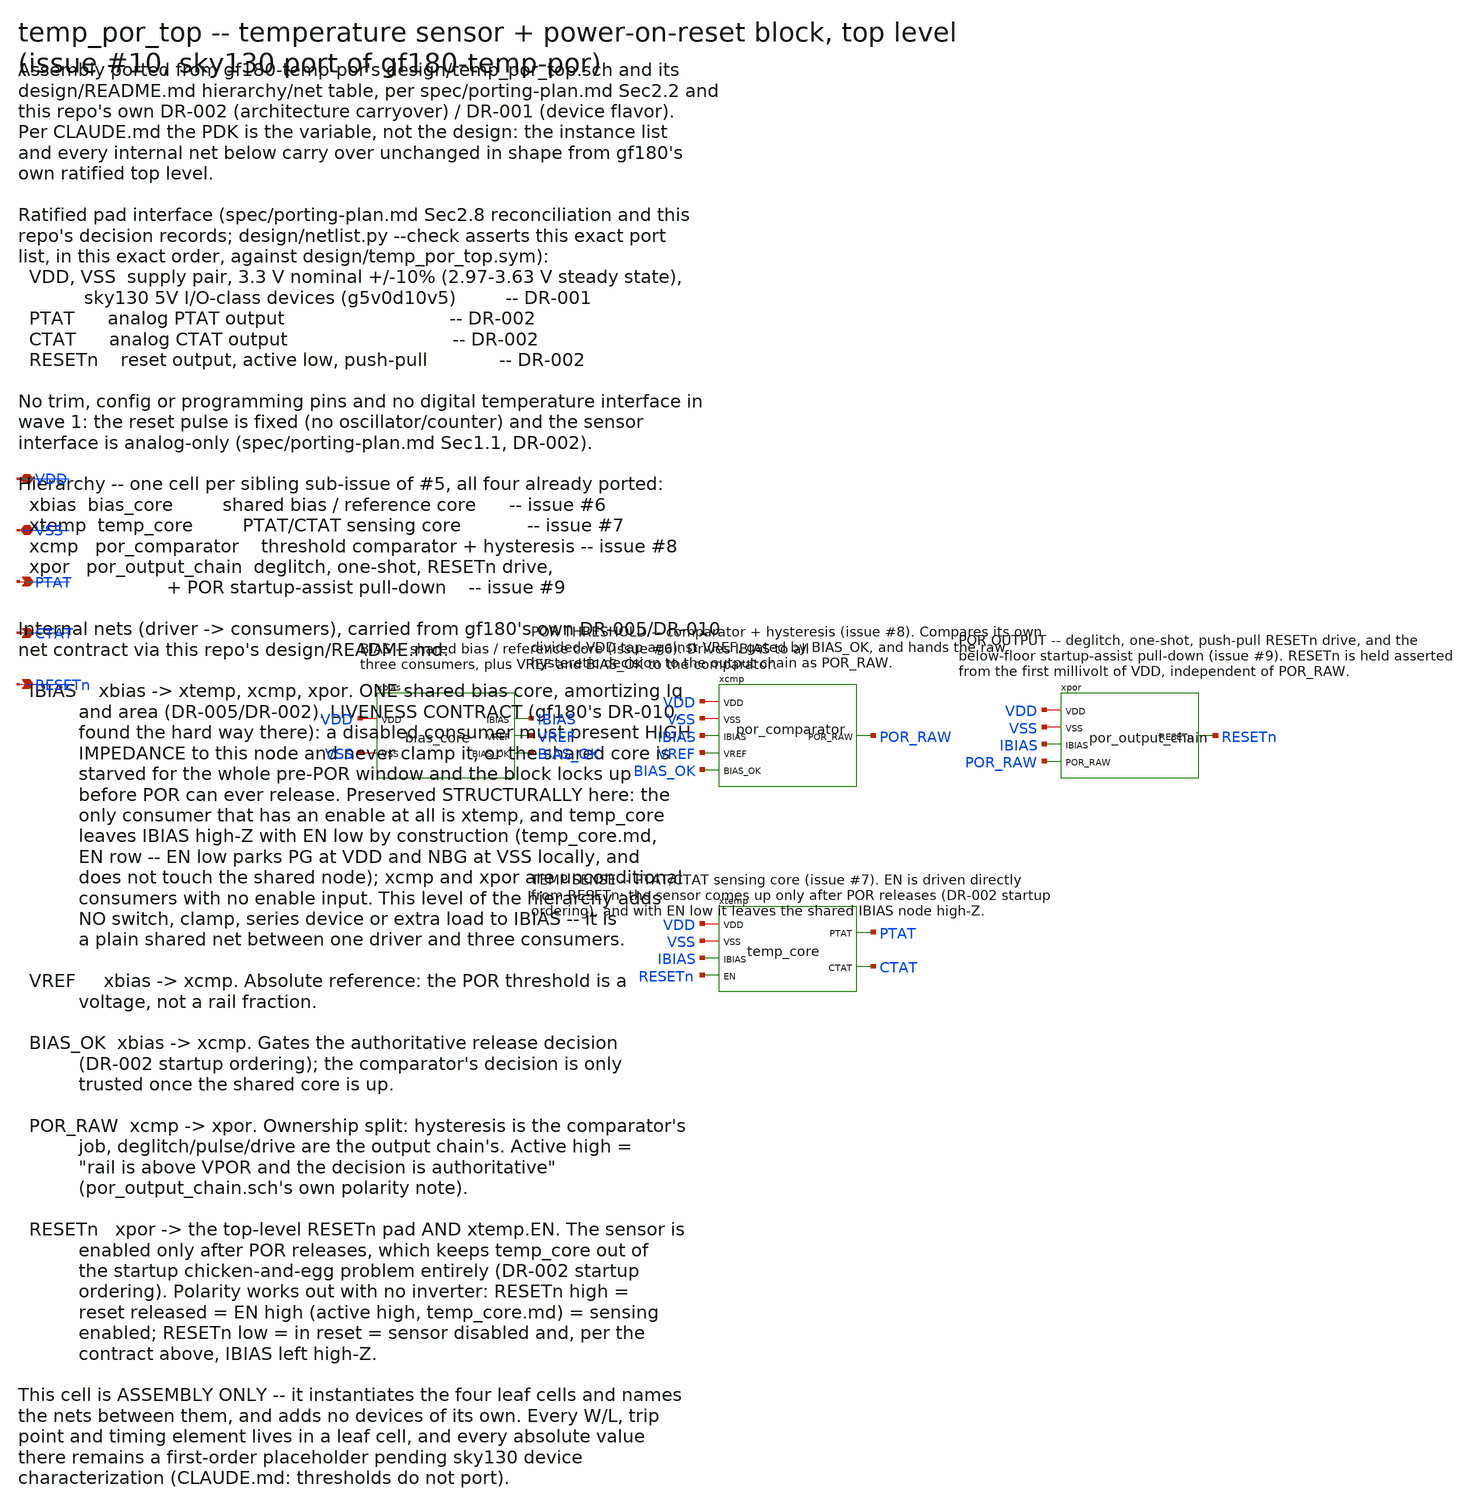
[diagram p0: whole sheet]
** sch_path: design/temp_por_top.sch
**.subckt temp_por_top VDD VSS PTAT CTAT RESETn
*.iopin VDD
*.iopin VSS
*.opin PTAT
*.opin CTAT
*.opin RESETn
xbias VDD VSS IBIAS VREF BIAS_OK bias_core
xcmp VDD VSS IBIAS VREF BIAS_OK POR_RAW por_comparator
xpor VDD VSS IBIAS POR_RAW RESETn por_output_chain
xtemp VDD VSS IBIAS RESETn PTAT CTAT temp_core
**.ends

* expanding   symbol:  bias_core.sym # of pins=5
** sym_path: bias_core.sym
** sch_path: bias_core.sch
.subckt bias_core VDD VSS IBIAS VREF BIAS_OK
*.iopin VDD
*.iopin VSS
*.opin IBIAS
*.opin VREF
*.opin BIAS_OK
XMP1 NA PG VDD VDD sky130_fd_pr__pfet_g5v0d10v5 L=4 W=8 nf=1 ad='int((1 + 1)/2) * 8 / 1 * 0.29' as='int((1 + 2)/2) * 8 / 1 * 0.29'
+ pd='2*int((1 + 1)/2) * (8 / 1 + 0.29)' ps='2*int((1 + 2)/2) * (8 / 1 + 0.29)' nrd='0.29 / 8 ' nrs='0.29 / 8 '
+ sa=0 sb=0 sd=0 mult=1 m=1
XMP2 NBTOP PG VDD VDD sky130_fd_pr__pfet_g5v0d10v5 L=4 W=8 nf=1 ad='int((1 + 1)/2) * 8 / 1 * 0.29' as='int((1 + 2)/2) * 8 / 1 * 0.29'
+ pd='2*int((1 + 1)/2) * (8 / 1 + 0.29)' ps='2*int((1 + 2)/2) * (8 / 1 + 0.29)' nrd='0.29 / 8 ' nrs='0.29 / 8 '
+ sa=0 sb=0 sd=0 mult=1 m=1
XMP3 VREF PG VDD VDD sky130_fd_pr__pfet_g5v0d10v5 L=4 W=8 nf=1 ad='int((1 + 1)/2) * 8 / 1 * 0.29' as='int((1 + 2)/2) * 8 / 1 * 0.29'
+ pd='2*int((1 + 1)/2) * (8 / 1 + 0.29)' ps='2*int((1 + 2)/2) * (8 / 1 + 0.29)' nrd='0.29 / 8 ' nrs='0.29 / 8 '
+ sa=0 sb=0 sd=0 mult=1 m=1
XMPBN NBG PG VDD VDD sky130_fd_pr__pfet_g5v0d10v5 L=4 W=2 nf=1 ad='int((1 + 1)/2) * 2 / 1 * 0.29' as='int((1 + 2)/2) * 2 / 1 * 0.29'
+ pd='2*int((1 + 1)/2) * (2 / 1 + 0.29)' ps='2*int((1 + 2)/2) * (2 / 1 + 0.29)' nrd='0.29 / 2 ' nrs='0.29 / 2 '
+ sa=0 sb=0 sd=0 mult=1 m=1
XQ1 VSS VSS NA sky130_fd_pr__pnp_05v5_W3p40L3p40 m=1
XRT NBTOP NB VSS sky130_fd_pr__res_xhigh_po W=2 L=17.5 mult=1 m=1
XR1 NB EC VSS sky130_fd_pr__res_xhigh_po W=2 L=350.0 mult=1 m=1
XQ8A VSS VSS EC sky130_fd_pr__pnp_05v5_W3p40L3p40 m=1
XQ8B VSS VSS EC sky130_fd_pr__pnp_05v5_W3p40L3p40 m=1
XQ8C VSS VSS EC sky130_fd_pr__pnp_05v5_W3p40L3p40 m=1
XQ8D VSS VSS EC sky130_fd_pr__pnp_05v5_W3p40L3p40 m=1
XQ8E VSS VSS EC sky130_fd_pr__pnp_05v5_W3p40L3p40 m=1
XQ8F VSS VSS EC sky130_fd_pr__pnp_05v5_W3p40L3p40 m=1
XQ8G VSS VSS EC sky130_fd_pr__pnp_05v5_W3p40L3p40 m=1
XQ8H VSS VSS EC sky130_fd_pr__pnp_05v5_W3p40L3p40 m=1
XR2 VREF ER VSS sky130_fd_pr__res_xhigh_po W=2 L=4104.0 mult=1 m=1
XQR VSS VSS ER sky130_fd_pr__pnp_05v5_W3p40L3p40 m=1
XMBN NBG NBG VSS VSS sky130_fd_pr__nfet_g5v0d10v5 L=4 W=2 nf=1 ad='int((1 + 1)/2) * 2 / 1 * 0.29' as='int((1 + 2)/2) * 2 / 1 * 0.29'
+ pd='2*int((1 + 1)/2) * (2 / 1 + 0.29)' ps='2*int((1 + 2)/2) * (2 / 1 + 0.29)' nrd='0.29 / 2 ' nrs='0.29 / 2 '
+ sa=0 sb=0 sd=0 mult=1 m=1
XMBN2 PB NBG VSS VSS sky130_fd_pr__nfet_g5v0d10v5 L=4 W=2 nf=1 ad='int((1 + 1)/2) * 2 / 1 * 0.29' as='int((1 + 2)/2) * 2 / 1 * 0.29'
+ pd='2*int((1 + 1)/2) * (2 / 1 + 0.29)' ps='2*int((1 + 2)/2) * (2 / 1 + 0.29)' nrd='0.29 / 2 ' nrs='0.29 / 2 '
+ sa=0 sb=0 sd=0 mult=1 m=1
XMBP PB PB VDD VDD sky130_fd_pr__pfet_g5v0d10v5 L=4 W=2 nf=1 ad='int((1 + 1)/2) * 2 / 1 * 0.29' as='int((1 + 2)/2) * 2 / 1 * 0.29'
+ pd='2*int((1 + 1)/2) * (2 / 1 + 0.29)' ps='2*int((1 + 2)/2) * (2 / 1 + 0.29)' nrd='0.29 / 2 ' nrs='0.29 / 2 '
+ sa=0 sb=0 sd=0 mult=1 m=1
XMPIB IBIAS PB VDD VDD sky130_fd_pr__pfet_g5v0d10v5 L=4 W=40 nf=1 ad='int((1 + 1)/2) * 40 / 1 * 0.29'
+ as='int((1 + 2)/2) * 40 / 1 * 0.29' pd='2*int((1 + 1)/2) * (40 / 1 + 0.29)' ps='2*int((1 + 2)/2) * (40 / 1 + 0.29)'
+ nrd='0.29 / 40 ' nrs='0.29 / 40 ' sa=0 sb=0 sd=0 mult=1 m=1
XMPT NT PB VDD VDD sky130_fd_pr__pfet_g5v0d10v5 L=4 W=2 nf=1 ad='int((1 + 1)/2) * 2 / 1 * 0.29' as='int((1 + 2)/2) * 2 / 1 * 0.29'
+ pd='2*int((1 + 1)/2) * (2 / 1 + 0.29)' ps='2*int((1 + 2)/2) * (2 / 1 + 0.29)' nrd='0.29 / 2 ' nrs='0.29 / 2 '
+ sa=0 sb=0 sd=0 mult=1 m=1
XMI1 N1 NA NT VDD sky130_fd_pr__pfet_g5v0d10v5 L=4 W=16 nf=1 ad='int((1 + 1)/2) * 16 / 1 * 0.29' as='int((1 + 2)/2) * 16 / 1 * 0.29'
+ pd='2*int((1 + 1)/2) * (16 / 1 + 0.29)' ps='2*int((1 + 2)/2) * (16 / 1 + 0.29)' nrd='0.29 / 16 ' nrs='0.29 / 16 '
+ sa=0 sb=0 sd=0 mult=1 m=1
XMI2 N2 NB NT VDD sky130_fd_pr__pfet_g5v0d10v5 L=4 W=16 nf=1 ad='int((1 + 1)/2) * 16 / 1 * 0.29' as='int((1 + 2)/2) * 16 / 1 * 0.29'
+ pd='2*int((1 + 1)/2) * (16 / 1 + 0.29)' ps='2*int((1 + 2)/2) * (16 / 1 + 0.29)' nrd='0.29 / 16 ' nrs='0.29 / 16 '
+ sa=0 sb=0 sd=0 mult=1 m=1
XML1 N1 N1 VSS VSS sky130_fd_pr__nfet_g5v0d10v5 L=8 W=4 nf=1 ad='int((1 + 1)/2) * 4 / 1 * 0.29' as='int((1 + 2)/2) * 4 / 1 * 0.29'
+ pd='2*int((1 + 1)/2) * (4 / 1 + 0.29)' ps='2*int((1 + 2)/2) * (4 / 1 + 0.29)' nrd='0.29 / 4 ' nrs='0.29 / 4 '
+ sa=0 sb=0 sd=0 mult=1 m=1
XML2 N2 N1 VSS VSS sky130_fd_pr__nfet_g5v0d10v5 L=8 W=4 nf=1 ad='int((1 + 1)/2) * 4 / 1 * 0.29' as='int((1 + 2)/2) * 4 / 1 * 0.29'
+ pd='2*int((1 + 1)/2) * (4 / 1 + 0.29)' ps='2*int((1 + 2)/2) * (4 / 1 + 0.29)' nrd='0.29 / 4 ' nrs='0.29 / 4 '
+ sa=0 sb=0 sd=0 mult=1 m=1
XMS2N PG N2 VSS VSS sky130_fd_pr__nfet_g5v0d10v5 L=8 W=8 nf=1 ad='int((1 + 1)/2) * 8 / 1 * 0.29' as='int((1 + 2)/2) * 8 / 1 * 0.29'
+ pd='2*int((1 + 1)/2) * (8 / 1 + 0.29)' ps='2*int((1 + 2)/2) * (8 / 1 + 0.29)' nrd='0.29 / 8 ' nrs='0.29 / 8 '
+ sa=0 sb=0 sd=0 mult=1 m=1
XMS2P PG PB VDD VDD sky130_fd_pr__pfet_g5v0d10v5 L=4 W=2 nf=1 ad='int((1 + 1)/2) * 2 / 1 * 0.29' as='int((1 + 2)/2) * 2 / 1 * 0.29'
+ pd='2*int((1 + 1)/2) * (2 / 1 + 0.29)' ps='2*int((1 + 2)/2) * (2 / 1 + 0.29)' nrd='0.29 / 2 ' nrs='0.29 / 2 '
+ sa=0 sb=0 sd=0 mult=1 m=1
XCC PG NZ sky130_fd_pr__cap_mim_m3_1 W=20 L=20 MF=1 m=1
XRZ NZ N2 VSS sky130_fd_pr__res_xhigh_po W=2 L=1016.0 mult=1 m=1
XKS0 VDD VDD KS1 VSS sky130_fd_pr__nfet_g5v0d10v5 L=8 W=1 nf=1 ad='int((1 + 1)/2) * 1 / 1 * 0.29' as='int((1 + 2)/2) * 1 / 1 * 0.29'
+ pd='2*int((1 + 1)/2) * (1 / 1 + 0.29)' ps='2*int((1 + 2)/2) * (1 / 1 + 0.29)' nrd='0.29 / 1 ' nrs='0.29 / 1 '
+ sa=0 sb=0 sd=0 mult=1 m=1
XKS1 KS1 KS1 KS2 VSS sky130_fd_pr__nfet_g5v0d10v5 L=8 W=1 nf=1 ad='int((1 + 1)/2) * 1 / 1 * 0.29' as='int((1 + 2)/2) * 1 / 1 * 0.29'
+ pd='2*int((1 + 1)/2) * (1 / 1 + 0.29)' ps='2*int((1 + 2)/2) * (1 / 1 + 0.29)' nrd='0.29 / 1 ' nrs='0.29 / 1 '
+ sa=0 sb=0 sd=0 mult=1 m=1
XKS2 KS2 KS2 KS3 VSS sky130_fd_pr__nfet_g5v0d10v5 L=8 W=1 nf=1 ad='int((1 + 1)/2) * 1 / 1 * 0.29' as='int((1 + 2)/2) * 1 / 1 * 0.29'
+ pd='2*int((1 + 1)/2) * (1 / 1 + 0.29)' ps='2*int((1 + 2)/2) * (1 / 1 + 0.29)' nrd='0.29 / 1 ' nrs='0.29 / 1 '
+ sa=0 sb=0 sd=0 mult=1 m=1
XKS3 KS3 KS3 KS4 VSS sky130_fd_pr__nfet_g5v0d10v5 L=8 W=1 nf=1 ad='int((1 + 1)/2) * 1 / 1 * 0.29' as='int((1 + 2)/2) * 1 / 1 * 0.29'
+ pd='2*int((1 + 1)/2) * (1 / 1 + 0.29)' ps='2*int((1 + 2)/2) * (1 / 1 + 0.29)' nrd='0.29 / 1 ' nrs='0.29 / 1 '
+ sa=0 sb=0 sd=0 mult=1 m=1
XKS4 KS4 KS4 NKG VSS sky130_fd_pr__nfet_g5v0d10v5 L=8 W=1 nf=1 ad='int((1 + 1)/2) * 1 / 1 * 0.29' as='int((1 + 2)/2) * 1 / 1 * 0.29'
+ pd='2*int((1 + 1)/2) * (1 / 1 + 0.29)' ps='2*int((1 + 2)/2) * (1 / 1 + 0.29)' nrd='0.29 / 1 ' nrs='0.29 / 1 '
+ sa=0 sb=0 sd=0 mult=1 m=1
XKA NKM PB VDD VDD sky130_fd_pr__pfet_g5v0d10v5 L=4 W=1 nf=1 ad='int((1 + 1)/2) * 1 / 1 * 0.29' as='int((1 + 2)/2) * 1 / 1 * 0.29'
+ pd='2*int((1 + 1)/2) * (1 / 1 + 0.29)' ps='2*int((1 + 2)/2) * (1 / 1 + 0.29)' nrd='0.29 / 1 ' nrs='0.29 / 1 '
+ sa=0 sb=0 sd=0 mult=1 m=1
XKAN NKM NKM VSS VSS sky130_fd_pr__nfet_g5v0d10v5 L=4 W=2 nf=1 ad='int((1 + 1)/2) * 2 / 1 * 0.29' as='int((1 + 2)/2) * 2 / 1 * 0.29'
+ pd='2*int((1 + 1)/2) * (2 / 1 + 0.29)' ps='2*int((1 + 2)/2) * (2 / 1 + 0.29)' nrd='0.29 / 2 ' nrs='0.29 / 2 '
+ sa=0 sb=0 sd=0 mult=1 m=1
XKPD NKG NKM VSS VSS sky130_fd_pr__nfet_g5v0d10v5 L=4 W=8 nf=1 ad='int((1 + 1)/2) * 8 / 1 * 0.29' as='int((1 + 2)/2) * 8 / 1 * 0.29'
+ pd='2*int((1 + 1)/2) * (8 / 1 + 0.29)' ps='2*int((1 + 2)/2) * (8 / 1 + 0.29)' nrd='0.29 / 8 ' nrs='0.29 / 8 '
+ sa=0 sb=0 sd=0 mult=1 m=1
XKICK PG NKG VSS VSS sky130_fd_pr__nfet_g5v0d10v5 L=4 W=1 nf=1 ad='int((1 + 1)/2) * 1 / 1 * 0.29' as='int((1 + 2)/2) * 1 / 1 * 0.29'
+ pd='2*int((1 + 1)/2) * (1 / 1 + 0.29)' ps='2*int((1 + 2)/2) * (1 / 1 + 0.29)' nrd='0.29 / 1 ' nrs='0.29 / 1 '
+ sa=0 sb=0 sd=0 mult=1 m=1
XMPOK TOK PB VDD VDD sky130_fd_pr__pfet_g5v0d10v5 L=4 W=1 nf=1 ad='int((1 + 1)/2) * 1 / 1 * 0.29' as='int((1 + 2)/2) * 1 / 1 * 0.29'
+ pd='2*int((1 + 1)/2) * (1 / 1 + 0.29)' ps='2*int((1 + 2)/2) * (1 / 1 + 0.29)' nrd='0.29 / 1 ' nrs='0.29 / 1 '
+ sa=0 sb=0 sd=0 mult=1 m=1
XMOKA NOKO NA TOK VDD sky130_fd_pr__pfet_g5v0d10v5 L=4 W=8 nf=1 ad='int((1 + 1)/2) * 8 / 1 * 0.29' as='int((1 + 2)/2) * 8 / 1 * 0.29'
+ pd='2*int((1 + 1)/2) * (8 / 1 + 0.29)' ps='2*int((1 + 2)/2) * (8 / 1 + 0.29)' nrd='0.29 / 8 ' nrs='0.29 / 8 '
+ sa=0 sb=0 sd=0 mult=1 m=1
XMOKB NOKL NBTOP TOK VDD sky130_fd_pr__pfet_g5v0d10v5 L=4 W=8 nf=1 ad='int((1 + 1)/2) * 8 / 1 * 0.29'
+ as='int((1 + 2)/2) * 8 / 1 * 0.29' pd='2*int((1 + 1)/2) * (8 / 1 + 0.29)' ps='2*int((1 + 2)/2) * (8 / 1 + 0.29)'
+ nrd='0.29 / 8 ' nrs='0.29 / 8 ' sa=0 sb=0 sd=0 mult=1 m=1
XMOL1 NOKL NOKL VSS VSS sky130_fd_pr__nfet_g5v0d10v5 L=4 W=2 nf=1 ad='int((1 + 1)/2) * 2 / 1 * 0.29'
+ as='int((1 + 2)/2) * 2 / 1 * 0.29' pd='2*int((1 + 1)/2) * (2 / 1 + 0.29)' ps='2*int((1 + 2)/2) * (2 / 1 + 0.29)'
+ nrd='0.29 / 2 ' nrs='0.29 / 2 ' sa=0 sb=0 sd=0 mult=1 m=1
XMOL2 NOKO NOKL VSS VSS sky130_fd_pr__nfet_g5v0d10v5 L=4 W=2 nf=1 ad='int((1 + 1)/2) * 2 / 1 * 0.29'
+ as='int((1 + 2)/2) * 2 / 1 * 0.29' pd='2*int((1 + 1)/2) * (2 / 1 + 0.29)' ps='2*int((1 + 2)/2) * (2 / 1 + 0.29)'
+ nrd='0.29 / 2 ' nrs='0.29 / 2 ' sa=0 sb=0 sd=0 mult=1 m=1
XMOKC NOKO NKG VSS VSS sky130_fd_pr__nfet_g5v0d10v5 L=1 W=2 nf=1 ad='int((1 + 1)/2) * 2 / 1 * 0.29' as='int((1 + 2)/2) * 2 / 1 * 0.29'
+ pd='2*int((1 + 1)/2) * (2 / 1 + 0.29)' ps='2*int((1 + 2)/2) * (2 / 1 + 0.29)' nrd='0.29 / 2 ' nrs='0.29 / 2 '
+ sa=0 sb=0 sd=0 mult=1 m=1
XMOK2 NOKX NOKO VSS VSS sky130_fd_pr__nfet_g5v0d10v5 L=4 W=2 nf=1 ad='int((1 + 1)/2) * 2 / 1 * 0.29'
+ as='int((1 + 2)/2) * 2 / 1 * 0.29' pd='2*int((1 + 1)/2) * (2 / 1 + 0.29)' ps='2*int((1 + 2)/2) * (2 / 1 + 0.29)'
+ nrd='0.29 / 2 ' nrs='0.29 / 2 ' sa=0 sb=0 sd=0 mult=1 m=1
XMOK2P NOKX PB VDD VDD sky130_fd_pr__pfet_g5v0d10v5 L=4 W=1 nf=1 ad='int((1 + 1)/2) * 1 / 1 * 0.29' as='int((1 + 2)/2) * 1 / 1 * 0.29'
+ pd='2*int((1 + 1)/2) * (1 / 1 + 0.29)' ps='2*int((1 + 2)/2) * (1 / 1 + 0.29)' nrd='0.29 / 1 ' nrs='0.29 / 1 '
+ sa=0 sb=0 sd=0 mult=1 m=1
XCOK VDD NOKX sky130_fd_pr__cap_mim_m3_1 W=6 L=6 MF=1 m=1
XMO1P BIAS_OK NOKX VDD VDD sky130_fd_pr__pfet_g5v0d10v5 L=4 W=1 nf=1 ad='int((1 + 1)/2) * 1 / 1 * 0.29'
+ as='int((1 + 2)/2) * 1 / 1 * 0.29' pd='2*int((1 + 1)/2) * (1 / 1 + 0.29)' ps='2*int((1 + 2)/2) * (1 / 1 + 0.29)'
+ nrd='0.29 / 1 ' nrs='0.29 / 1 ' sa=0 sb=0 sd=0 mult=1 m=1
XMO1N BIAS_OK NOKX VSS VSS sky130_fd_pr__nfet_g5v0d10v5 L=0.5 W=4 nf=1 ad='int((1 + 1)/2) * 4 / 1 * 0.29'
+ as='int((1 + 2)/2) * 4 / 1 * 0.29' pd='2*int((1 + 1)/2) * (4 / 1 + 0.29)' ps='2*int((1 + 2)/2) * (4 / 1 + 0.29)'
+ nrd='0.29 / 4 ' nrs='0.29 / 4 ' sa=0 sb=0 sd=0 mult=1 m=1
.ends


* expanding   symbol:  por_comparator.sym # of pins=6
** sym_path: por_comparator.sym
** sch_path: por_comparator.sch
.subckt por_comparator VDD VSS IBIAS VREF BIAS_OK POR_RAW
*.iopin VDD
*.iopin VSS
*.ipin IBIAS
*.ipin VREF
*.ipin BIAS_OK
*.opin POR_RAW
XMENP BIAS_OKB BIAS_OK VDD VDD sky130_fd_pr__pfet_g5v0d10v5 L=0.5 W=2 nf=1 ad='int((1 + 1)/2) * 2 / 1 * 0.29'
+ as='int((1 + 2)/2) * 2 / 1 * 0.29' pd='2*int((1 + 1)/2) * (2 / 1 + 0.29)' ps='2*int((1 + 2)/2) * (2 / 1 + 0.29)'
+ nrd='0.29 / 2 ' nrs='0.29 / 2 ' sa=0 sb=0 sd=0 mult=1 m=1
XMENN BIAS_OKB BIAS_OK VSS VSS sky130_fd_pr__nfet_g5v0d10v5 L=0.5 W=1 nf=1 ad='int((1 + 1)/2) * 1 / 1 * 0.29'
+ as='int((1 + 2)/2) * 1 / 1 * 0.29' pd='2*int((1 + 1)/2) * (1 / 1 + 0.29)' ps='2*int((1 + 2)/2) * (1 / 1 + 0.29)'
+ nrd='0.29 / 1 ' nrs='0.29 / 1 ' sa=0 sb=0 sd=0 mult=1 m=1
XMBD IBIAS NBG VSS VSS sky130_fd_pr__nfet_g5v0d10v5 L=2 W=2 nf=1 ad='int((1 + 1)/2) * 2 / 1 * 0.29' as='int((1 + 2)/2) * 2 / 1 * 0.29'
+ pd='2*int((1 + 1)/2) * (2 / 1 + 0.29)' ps='2*int((1 + 2)/2) * (2 / 1 + 0.29)' nrd='0.29 / 2 ' nrs='0.29 / 2 '
+ sa=0 sb=0 sd=0 mult=1 m=1
XMPASS IBIAS BIAS_OK NBG VSS sky130_fd_pr__nfet_g5v0d10v5 L=0.5 W=2 nf=1 ad='int((1 + 1)/2) * 2 / 1 * 0.29'
+ as='int((1 + 2)/2) * 2 / 1 * 0.29' pd='2*int((1 + 1)/2) * (2 / 1 + 0.29)' ps='2*int((1 + 2)/2) * (2 / 1 + 0.29)'
+ nrd='0.29 / 2 ' nrs='0.29 / 2 ' sa=0 sb=0 sd=0 mult=1 m=1
XMDNB NBG BIAS_OKB VSS VSS sky130_fd_pr__nfet_g5v0d10v5 L=0.5 W=2 nf=1 ad='int((1 + 1)/2) * 2 / 1 * 0.29'
+ as='int((1 + 2)/2) * 2 / 1 * 0.29' pd='2*int((1 + 1)/2) * (2 / 1 + 0.29)' ps='2*int((1 + 2)/2) * (2 / 1 + 0.29)'
+ nrd='0.29 / 2 ' nrs='0.29 / 2 ' sa=0 sb=0 sd=0 mult=1 m=1
XMDIB IBIAS BIAS_OKB VSS VSS sky130_fd_pr__nfet_g5v0d10v5 L=1 W=1 nf=1 ad='int((1 + 1)/2) * 1 / 1 * 0.29'
+ as='int((1 + 2)/2) * 1 / 1 * 0.29' pd='2*int((1 + 1)/2) * (1 / 1 + 0.29)' ps='2*int((1 + 2)/2) * (1 / 1 + 0.29)'
+ nrd='0.29 / 1 ' nrs='0.29 / 1 ' sa=0 sb=0 sd=0 mult=1 m=1
XRTOP SNS VDD VSS sky130_fd_pr__res_xhigh_po W=2 L=7897.44 mult=1 m=1
XRBOT SNSB SNS VSS sky130_fd_pr__res_xhigh_po W=2 L=6769.23 mult=1 m=1
XRHYS VSS SNSB VSS sky130_fd_pr__res_xhigh_po W=2 L=775.0 mult=1 m=1
XMHSW SNSB N1 VSS VSS sky130_fd_pr__nfet_g5v0d10v5 L=0.5 W=10 nf=1 ad='int((1 + 1)/2) * 10 / 1 * 0.29'
+ as='int((1 + 2)/2) * 10 / 1 * 0.29' pd='2*int((1 + 1)/2) * (10 / 1 + 0.29)' ps='2*int((1 + 2)/2) * (10 / 1 + 0.29)'
+ nrd='0.29 / 10 ' nrs='0.29 / 10 ' sa=0 sb=0 sd=0 mult=1 m=1
XMTAIL TN NBG VSS VSS sky130_fd_pr__nfet_g5v0d10v5 L=10 W=1 nf=1 ad='int((1 + 1)/2) * 1 / 1 * 0.29' as='int((1 + 2)/2) * 1 / 1 * 0.29'
+ pd='2*int((1 + 1)/2) * (1 / 1 + 0.29)' ps='2*int((1 + 2)/2) * (1 / 1 + 0.29)' nrd='0.29 / 1 ' nrs='0.29 / 1 '
+ sa=0 sb=0 sd=0 mult=1 m=1
XMINA NA SNS TN VSS sky130_fd_pr__nfet_g5v0d10v5 L=1 W=2 nf=1 ad='int((1 + 1)/2) * 2 / 1 * 0.29' as='int((1 + 2)/2) * 2 / 1 * 0.29'
+ pd='2*int((1 + 1)/2) * (2 / 1 + 0.29)' ps='2*int((1 + 2)/2) * (2 / 1 + 0.29)' nrd='0.29 / 2 ' nrs='0.29 / 2 '
+ sa=0 sb=0 sd=0 mult=1 m=1
XMINB CMPO VREF TN VSS sky130_fd_pr__nfet_g5v0d10v5 L=1 W=2 nf=1 ad='int((1 + 1)/2) * 2 / 1 * 0.29' as='int((1 + 2)/2) * 2 / 1 * 0.29'
+ pd='2*int((1 + 1)/2) * (2 / 1 + 0.29)' ps='2*int((1 + 2)/2) * (2 / 1 + 0.29)' nrd='0.29 / 2 ' nrs='0.29 / 2 '
+ sa=0 sb=0 sd=0 mult=1 m=1
XMLA NA NA VDDA VDD sky130_fd_pr__pfet_g5v0d10v5 L=1 W=4 nf=1 ad='int((1 + 1)/2) * 4 / 1 * 0.29' as='int((1 + 2)/2) * 4 / 1 * 0.29'
+ pd='2*int((1 + 1)/2) * (4 / 1 + 0.29)' ps='2*int((1 + 2)/2) * (4 / 1 + 0.29)' nrd='0.29 / 4 ' nrs='0.29 / 4 '
+ sa=0 sb=0 sd=0 mult=1 m=1
XMLB CMPO NA VDDA VDD sky130_fd_pr__pfet_g5v0d10v5 L=1 W=4 nf=1 ad='int((1 + 1)/2) * 4 / 1 * 0.29' as='int((1 + 2)/2) * 4 / 1 * 0.29'
+ pd='2*int((1 + 1)/2) * (4 / 1 + 0.29)' ps='2*int((1 + 2)/2) * (4 / 1 + 0.29)' nrd='0.29 / 4 ' nrs='0.29 / 4 '
+ sa=0 sb=0 sd=0 mult=1 m=1
XMENSRC VDDA BIAS_OKB VDD VDD sky130_fd_pr__pfet_g5v0d10v5 L=0.5 W=4 nf=1 ad='int((1 + 1)/2) * 4 / 1 * 0.29'
+ as='int((1 + 2)/2) * 4 / 1 * 0.29' pd='2*int((1 + 1)/2) * (4 / 1 + 0.29)' ps='2*int((1 + 2)/2) * (4 / 1 + 0.29)'
+ nrd='0.29 / 4 ' nrs='0.29 / 4 ' sa=0 sb=0 sd=0 mult=1 m=1
XMDCMPO CMPO BIAS_OKB VSS VSS sky130_fd_pr__nfet_g5v0d10v5 L=1 W=2 nf=1 ad='int((1 + 1)/2) * 2 / 1 * 0.29'
+ as='int((1 + 2)/2) * 2 / 1 * 0.29' pd='2*int((1 + 1)/2) * (2 / 1 + 0.29)' ps='2*int((1 + 2)/2) * (2 / 1 + 0.29)'
+ nrd='0.29 / 2 ' nrs='0.29 / 2 ' sa=0 sb=0 sd=0 mult=1 m=1
XMI1P N1 CMPO VDD VDD sky130_fd_pr__pfet_g5v0d10v5 L=0.5 W=2 nf=1 ad='int((1 + 1)/2) * 2 / 1 * 0.29'
+ as='int((1 + 2)/2) * 2 / 1 * 0.29' pd='2*int((1 + 1)/2) * (2 / 1 + 0.29)' ps='2*int((1 + 2)/2) * (2 / 1 + 0.29)'
+ nrd='0.29 / 2 ' nrs='0.29 / 2 ' sa=0 sb=0 sd=0 mult=1 m=1
XMI1N N1 CMPO VSS VSS sky130_fd_pr__nfet_g5v0d10v5 L=0.5 W=1 nf=1 ad='int((1 + 1)/2) * 1 / 1 * 0.29'
+ as='int((1 + 2)/2) * 1 / 1 * 0.29' pd='2*int((1 + 1)/2) * (1 / 1 + 0.29)' ps='2*int((1 + 2)/2) * (1 / 1 + 0.29)'
+ nrd='0.29 / 1 ' nrs='0.29 / 1 ' sa=0 sb=0 sd=0 mult=1 m=1
XMI2P POR_RAW N1 VDD VDD sky130_fd_pr__pfet_g5v0d10v5 L=0.5 W=2 nf=1 ad='int((1 + 1)/2) * 2 / 1 * 0.29'
+ as='int((1 + 2)/2) * 2 / 1 * 0.29' pd='2*int((1 + 1)/2) * (2 / 1 + 0.29)' ps='2*int((1 + 2)/2) * (2 / 1 + 0.29)'
+ nrd='0.29 / 2 ' nrs='0.29 / 2 ' sa=0 sb=0 sd=0 mult=1 m=1
XMI2N POR_RAW N1 VSS VSS sky130_fd_pr__nfet_g5v0d10v5 L=0.5 W=1 nf=1 ad='int((1 + 1)/2) * 1 / 1 * 0.29'
+ as='int((1 + 2)/2) * 1 / 1 * 0.29' pd='2*int((1 + 1)/2) * (1 / 1 + 0.29)' ps='2*int((1 + 2)/2) * (1 / 1 + 0.29)'
+ nrd='0.29 / 1 ' nrs='0.29 / 1 ' sa=0 sb=0 sd=0 mult=1 m=1
.ends


* expanding   symbol:  por_output_chain.sym # of pins=5
** sym_path: design/por_output_chain.sym
** sch_path: design/por_output_chain.sch
.subckt por_output_chain VDD VSS IBIAS POR_RAW RESETn
*.iopin VDD
*.iopin VSS
*.ipin IBIAS
*.ipin POR_RAW
*.opin RESETn
XMBD IBIAS IBIAS VSS VSS sky130_fd_pr__nfet_g5v0d10v5 L=4 W=4 nf=1 ad='int((1 + 1)/2) * 4 / 1 * 0.29'
+ as='int((1 + 2)/2) * 4 / 1 * 0.29' pd='2*int((1 + 1)/2) * (4 / 1 + 0.29)' ps='2*int((1 + 2)/2) * (4 / 1 + 0.29)'
+ nrd='0.29 / 4 ' nrs='0.29 / 4 ' sa=0 sb=0 sd=0 mult=1 m=1
XMN1 PDN IBIAS VSS VSS sky130_fd_pr__nfet_g5v0d10v5 L=20 W=0.42 nf=1 ad='int((1 + 1)/2) * 0.42 / 1 * 0.29'
+ as='int((1 + 2)/2) * 0.42 / 1 * 0.29' pd='2*int((1 + 1)/2) * (0.42 / 1 + 0.29)' ps='2*int((1 + 2)/2) * (0.42 / 1 + 0.29)'
+ nrd='0.29 / 0.42 ' nrs='0.29 / 0.42 ' sa=0 sb=0 sd=0 mult=1 m=1
XMPD PDN PDN VDD VDD sky130_fd_pr__pfet_g5v0d10v5 L=10 W=2 nf=1 ad='int((1 + 1)/2) * 2 / 1 * 0.29' as='int((1 + 2)/2) * 2 / 1 * 0.29'
+ pd='2*int((1 + 1)/2) * (2 / 1 + 0.29)' ps='2*int((1 + 2)/2) * (2 / 1 + 0.29)' nrd='0.29 / 2 ' nrs='0.29 / 2 '
+ sa=0 sb=0 sd=0 mult=1 m=1
XMP2 NDL PDN VDD VDD sky130_fd_pr__pfet_g5v0d10v5 L=10 W=2 nf=1 ad='int((1 + 1)/2) * 2 / 1 * 0.29' as='int((1 + 2)/2) * 2 / 1 * 0.29'
+ pd='2*int((1 + 1)/2) * (2 / 1 + 0.29)' ps='2*int((1 + 2)/2) * (2 / 1 + 0.29)' nrd='0.29 / 2 ' nrs='0.29 / 2 '
+ sa=0 sb=0 sd=0 mult=1 m=1
XMND NDL NDL VSS VSS sky130_fd_pr__nfet_g5v0d10v5 L=10 W=2 nf=1 ad='int((1 + 1)/2) * 2 / 1 * 0.29' as='int((1 + 2)/2) * 2 / 1 * 0.29'
+ pd='2*int((1 + 1)/2) * (2 / 1 + 0.29)' ps='2*int((1 + 2)/2) * (2 / 1 + 0.29)' nrd='0.29 / 2 ' nrs='0.29 / 2 '
+ sa=0 sb=0 sd=0 mult=1 m=1
XMDGPT NDGP PDN VDD VDD sky130_fd_pr__pfet_g5v0d10v5 L=10 W=10 nf=1 ad='int((1 + 1)/2) * 10 / 1 * 0.29'
+ as='int((1 + 2)/2) * 10 / 1 * 0.29' pd='2*int((1 + 1)/2) * (10 / 1 + 0.29)' ps='2*int((1 + 2)/2) * (10 / 1 + 0.29)'
+ nrd='0.29 / 10 ' nrs='0.29 / 10 ' sa=0 sb=0 sd=0 mult=1 m=1
XMDGPI NDG POR_RAW NDGP VDD sky130_fd_pr__pfet_g5v0d10v5 L=0.5 W=1 nf=1 ad='int((1 + 1)/2) * 1 / 1 * 0.29'
+ as='int((1 + 2)/2) * 1 / 1 * 0.29' pd='2*int((1 + 1)/2) * (1 / 1 + 0.29)' ps='2*int((1 + 2)/2) * (1 / 1 + 0.29)'
+ nrd='0.29 / 1 ' nrs='0.29 / 1 ' sa=0 sb=0 sd=0 mult=1 m=1
XMDGNI NDG POR_RAW NDGN VSS sky130_fd_pr__nfet_g5v0d10v5 L=0.5 W=1 nf=1 ad='int((1 + 1)/2) * 1 / 1 * 0.29'
+ as='int((1 + 2)/2) * 1 / 1 * 0.29' pd='2*int((1 + 1)/2) * (1 / 1 + 0.29)' ps='2*int((1 + 2)/2) * (1 / 1 + 0.29)'
+ nrd='0.29 / 1 ' nrs='0.29 / 1 ' sa=0 sb=0 sd=0 mult=1 m=1
XMDGNT NDGN NDL VSS VSS sky130_fd_pr__nfet_g5v0d10v5 L=10 W=10 nf=1 ad='int((1 + 1)/2) * 10 / 1 * 0.29'
+ as='int((1 + 2)/2) * 10 / 1 * 0.29' pd='2*int((1 + 1)/2) * (10 / 1 + 0.29)' ps='2*int((1 + 2)/2) * (10 / 1 + 0.29)'
+ nrd='0.29 / 10 ' nrs='0.29 / 10 ' sa=0 sb=0 sd=0 mult=1 m=1
XCDG NDG VSS sky130_fd_pr__cap_mim_m3_1 W=11 L=11 MF=1 m=1
XMG1P PGDG NDG VDD VDD sky130_fd_pr__pfet_g5v0d10v5 L=2 W=0.5 nf=1 ad='int((1 + 1)/2) * 0.5 / 1 * 0.29'
+ as='int((1 + 2)/2) * 0.5 / 1 * 0.29' pd='2*int((1 + 1)/2) * (0.5 / 1 + 0.29)' ps='2*int((1 + 2)/2) * (0.5 / 1 + 0.29)'
+ nrd='0.29 / 0.5 ' nrs='0.29 / 0.5 ' sa=0 sb=0 sd=0 mult=1 m=1
XMG1N PGDG NDG VSS VSS sky130_fd_pr__nfet_g5v0d10v5 L=0.5 W=2 nf=1 ad='int((1 + 1)/2) * 2 / 1 * 0.29'
+ as='int((1 + 2)/2) * 2 / 1 * 0.29' pd='2*int((1 + 1)/2) * (2 / 1 + 0.29)' ps='2*int((1 + 2)/2) * (2 / 1 + 0.29)'
+ nrd='0.29 / 2 ' nrs='0.29 / 2 ' sa=0 sb=0 sd=0 mult=1 m=1
XMG2P PGDGB PGDG VDD VDD sky130_fd_pr__pfet_g5v0d10v5 L=0.5 W=2 nf=1 ad='int((1 + 1)/2) * 2 / 1 * 0.29'
+ as='int((1 + 2)/2) * 2 / 1 * 0.29' pd='2*int((1 + 1)/2) * (2 / 1 + 0.29)' ps='2*int((1 + 2)/2) * (2 / 1 + 0.29)'
+ nrd='0.29 / 2 ' nrs='0.29 / 2 ' sa=0 sb=0 sd=0 mult=1 m=1
XMG2N PGDGB PGDG VSS VSS sky130_fd_pr__nfet_g5v0d10v5 L=2 W=0.5 nf=1 ad='int((1 + 1)/2) * 0.5 / 1 * 0.29'
+ as='int((1 + 2)/2) * 0.5 / 1 * 0.29' pd='2*int((1 + 1)/2) * (0.5 / 1 + 0.29)' ps='2*int((1 + 2)/2) * (0.5 / 1 + 0.29)'
+ nrd='0.29 / 0.5 ' nrs='0.29 / 0.5 ' sa=0 sb=0 sd=0 mult=1 m=1
XMPT NTS PDN VDD VDD sky130_fd_pr__pfet_g5v0d10v5 L=10 W=0.5 nf=1 ad='int((1 + 1)/2) * 0.5 / 1 * 0.29'
+ as='int((1 + 2)/2) * 0.5 / 1 * 0.29' pd='2*int((1 + 1)/2) * (0.5 / 1 + 0.29)' ps='2*int((1 + 2)/2) * (0.5 / 1 + 0.29)'
+ nrd='0.29 / 0.5 ' nrs='0.29 / 0.5 ' sa=0 sb=0 sd=0 mult=1 m=1
XMTSW TIM PGDGB NTS VDD sky130_fd_pr__pfet_g5v0d10v5 L=1 W=2 nf=1 ad='int((1 + 1)/2) * 2 / 1 * 0.29'
+ as='int((1 + 2)/2) * 2 / 1 * 0.29' pd='2*int((1 + 1)/2) * (2 / 1 + 0.29)' ps='2*int((1 + 2)/2) * (2 / 1 + 0.29)'
+ nrd='0.29 / 2 ' nrs='0.29 / 2 ' sa=0 sb=0 sd=0 mult=1 m=1
XMDIS TIM PGDGB VSS VSS sky130_fd_pr__nfet_g5v0d10v5 L=1 W=1 nf=1 ad='int((1 + 1)/2) * 1 / 1 * 0.29'
+ as='int((1 + 2)/2) * 1 / 1 * 0.29' pd='2*int((1 + 1)/2) * (1 / 1 + 0.29)' ps='2*int((1 + 2)/2) * (1 / 1 + 0.29)'
+ nrd='0.29 / 1 ' nrs='0.29 / 1 ' sa=0 sb=0 sd=0 mult=1 m=1
XCTIM TIM VSS sky130_fd_pr__cap_mim_m3_1 W=28 L=28 MF=4 m=4
XMDAPI ND1 TIM VDD VDD sky130_fd_pr__pfet_g5v0d10v5 L=1 W=2 nf=1 ad='int((1 + 1)/2) * 2 / 1 * 0.29' as='int((1 + 2)/2) * 2 / 1 * 0.29'
+ pd='2*int((1 + 1)/2) * (2 / 1 + 0.29)' ps='2*int((1 + 2)/2) * (2 / 1 + 0.29)' nrd='0.29 / 2 ' nrs='0.29 / 2 '
+ sa=0 sb=0 sd=0 mult=1 m=1
XMDANT ND1 NDL VSS VSS sky130_fd_pr__nfet_g5v0d10v5 L=10 W=0.5 nf=1 ad='int((1 + 1)/2) * 0.5 / 1 * 0.29'
+ as='int((1 + 2)/2) * 0.5 / 1 * 0.29' pd='2*int((1 + 1)/2) * (0.5 / 1 + 0.29)' ps='2*int((1 + 2)/2) * (0.5 / 1 + 0.29)'
+ nrd='0.29 / 0.5 ' nrs='0.29 / 0.5 ' sa=0 sb=0 sd=0 mult=1 m=1
XMDBNI TRIP ND1 VSS VSS sky130_fd_pr__nfet_g5v0d10v5 L=1 W=1 nf=1 ad='int((1 + 1)/2) * 1 / 1 * 0.29'
+ as='int((1 + 2)/2) * 1 / 1 * 0.29' pd='2*int((1 + 1)/2) * (1 / 1 + 0.29)' ps='2*int((1 + 2)/2) * (1 / 1 + 0.29)'
+ nrd='0.29 / 1 ' nrs='0.29 / 1 ' sa=0 sb=0 sd=0 mult=1 m=1
XMDBPT TRIP PDN VDD VDD sky130_fd_pr__pfet_g5v0d10v5 L=10 W=0.5 nf=1 ad='int((1 + 1)/2) * 0.5 / 1 * 0.29'
+ as='int((1 + 2)/2) * 0.5 / 1 * 0.29' pd='2*int((1 + 1)/2) * (0.5 / 1 + 0.29)' ps='2*int((1 + 2)/2) * (0.5 / 1 + 0.29)'
+ nrd='0.29 / 0.5 ' nrs='0.29 / 0.5 ' sa=0 sb=0 sd=0 mult=1 m=1
XMRLK ND1 RESETn VSS VSS sky130_fd_pr__nfet_g5v0d10v5 L=1 W=1 nf=1 ad='int((1 + 1)/2) * 1 / 1 * 0.29'
+ as='int((1 + 2)/2) * 1 / 1 * 0.29' pd='2*int((1 + 1)/2) * (1 / 1 + 0.29)' ps='2*int((1 + 2)/2) * (1 / 1 + 0.29)'
+ nrd='0.29 / 1 ' nrs='0.29 / 1 ' sa=0 sb=0 sd=0 mult=1 m=1
XMNAP1 RSTB TRIP VDD VDD sky130_fd_pr__pfet_g5v0d10v5 L=0.5 W=4 nf=1 ad='int((1 + 1)/2) * 4 / 1 * 0.29'
+ as='int((1 + 2)/2) * 4 / 1 * 0.29' pd='2*int((1 + 1)/2) * (4 / 1 + 0.29)' ps='2*int((1 + 2)/2) * (4 / 1 + 0.29)'
+ nrd='0.29 / 4 ' nrs='0.29 / 4 ' sa=0 sb=0 sd=0 mult=1 m=1
XMNAP2 RSTB PGDG VDD VDD sky130_fd_pr__pfet_g5v0d10v5 L=0.5 W=4 nf=1 ad='int((1 + 1)/2) * 4 / 1 * 0.29'
+ as='int((1 + 2)/2) * 4 / 1 * 0.29' pd='2*int((1 + 1)/2) * (4 / 1 + 0.29)' ps='2*int((1 + 2)/2) * (4 / 1 + 0.29)'
+ nrd='0.29 / 4 ' nrs='0.29 / 4 ' sa=0 sb=0 sd=0 mult=1 m=1
XMNAN1 RSTB TRIP NNAND VSS sky130_fd_pr__nfet_g5v0d10v5 L=0.5 W=2 nf=1 ad='int((1 + 1)/2) * 2 / 1 * 0.29'
+ as='int((1 + 2)/2) * 2 / 1 * 0.29' pd='2*int((1 + 1)/2) * (2 / 1 + 0.29)' ps='2*int((1 + 2)/2) * (2 / 1 + 0.29)'
+ nrd='0.29 / 2 ' nrs='0.29 / 2 ' sa=0 sb=0 sd=0 mult=1 m=1
XMNAN2 NNAND PGDG VSS VSS sky130_fd_pr__nfet_g5v0d10v5 L=0.5 W=2 nf=1 ad='int((1 + 1)/2) * 2 / 1 * 0.29'
+ as='int((1 + 2)/2) * 2 / 1 * 0.29' pd='2*int((1 + 1)/2) * (2 / 1 + 0.29)' ps='2*int((1 + 2)/2) * (2 / 1 + 0.29)'
+ nrd='0.29 / 2 ' nrs='0.29 / 2 ' sa=0 sb=0 sd=0 mult=1 m=1
XMAST RSTB RESETn VDD VDD sky130_fd_pr__pfet_g5v0d10v5 L=10 W=0.5 nf=1 ad='int((1 + 1)/2) * 0.5 / 1 * 0.29'
+ as='int((1 + 2)/2) * 0.5 / 1 * 0.29' pd='2*int((1 + 1)/2) * (0.5 / 1 + 0.29)' ps='2*int((1 + 2)/2) * (0.5 / 1 + 0.29)'
+ nrd='0.29 / 0.5 ' nrs='0.29 / 0.5 ' sa=0 sb=0 sd=0 mult=1 m=1
XMOP RESETn RSTB VDD VDD sky130_fd_pr__pfet_g5v0d10v5 L=1 W=1 nf=1 ad='int((1 + 1)/2) * 1 / 1 * 0.29'
+ as='int((1 + 2)/2) * 1 / 1 * 0.29' pd='2*int((1 + 1)/2) * (1 / 1 + 0.29)' ps='2*int((1 + 2)/2) * (1 / 1 + 0.29)'
+ nrd='0.29 / 1 ' nrs='0.29 / 1 ' sa=0 sb=0 sd=0 mult=1 m=1
XMON RESETn RSTB VSS VSS sky130_fd_pr__nfet_g5v0d10v5 L=0.5 W=10 nf=1 ad='int((1 + 1)/2) * 10 / 1 * 0.29'
+ as='int((1 + 2)/2) * 10 / 1 * 0.29' pd='2*int((1 + 1)/2) * (10 / 1 + 0.29)' ps='2*int((1 + 2)/2) * (10 / 1 + 0.29)'
+ nrd='0.29 / 10 ' nrs='0.29 / 10 ' sa=0 sb=0 sd=0 mult=1 m=1
XMASSIST RESETn VDD VSS VSS sky130_fd_pr__nfet_05v0_nvt L=25 W=1 nf=1 ad='int((1 + 1)/2) * 1 / 1 * 0.29'
+ as='int((1 + 2)/2) * 1 / 1 * 0.29' pd='2*int((1 + 1)/2) * (1 / 1 + 0.29)' ps='2*int((1 + 2)/2) * (1 / 1 + 0.29)'
+ nrd='0.29 / 1 ' nrs='0.29 / 1 ' sa=0 sb=0 sd=0 mult=1 m=1
.ends


* expanding   symbol:  temp_core.sym # of pins=6
** sym_path: temp_core.sym
** sch_path: temp_core.sch
.subckt temp_core VDD VSS IBIAS EN PTAT CTAT
*.iopin VDD
*.iopin VSS
*.ipin IBIAS
*.ipin EN
*.opin PTAT
*.opin CTAT
XMBD IBIAS NBG VSS VSS sky130_fd_pr__nfet_g5v0d10v5 L=2 W=4 nf=1 ad='int((1 + 1)/2) * 4 / 1 * 0.29' as='int((1 + 2)/2) * 4 / 1 * 0.29'
+ pd='2*int((1 + 1)/2) * (4 / 1 + 0.29)' ps='2*int((1 + 2)/2) * (4 / 1 + 0.29)' nrd='0.29 / 4 ' nrs='0.29 / 4 '
+ sa=0 sb=0 sd=0 mult=1 m=1
XMPASS IBIAS EN NBG VSS sky130_fd_pr__nfet_g5v0d10v5 L=0.5 W=2 nf=1 ad='int((1 + 1)/2) * 2 / 1 * 0.29'
+ as='int((1 + 2)/2) * 2 / 1 * 0.29' pd='2*int((1 + 1)/2) * (2 / 1 + 0.29)' ps='2*int((1 + 2)/2) * (2 / 1 + 0.29)'
+ nrd='0.29 / 2 ' nrs='0.29 / 2 ' sa=0 sb=0 sd=0 mult=1 m=1
XMDNB NBG ENB VSS VSS sky130_fd_pr__nfet_g5v0d10v5 L=0.5 W=2 nf=1 ad='int((1 + 1)/2) * 2 / 1 * 0.29'
+ as='int((1 + 2)/2) * 2 / 1 * 0.29' pd='2*int((1 + 1)/2) * (2 / 1 + 0.29)' ps='2*int((1 + 2)/2) * (2 / 1 + 0.29)'
+ nrd='0.29 / 2 ' nrs='0.29 / 2 ' sa=0 sb=0 sd=0 mult=1 m=1
XMBN1 PB NBG VSS VSS sky130_fd_pr__nfet_g5v0d10v5 L=2 W=4 nf=1 ad='int((1 + 1)/2) * 4 / 1 * 0.29' as='int((1 + 2)/2) * 4 / 1 * 0.29'
+ pd='2*int((1 + 1)/2) * (4 / 1 + 0.29)' ps='2*int((1 + 2)/2) * (4 / 1 + 0.29)' nrd='0.29 / 4 ' nrs='0.29 / 4 '
+ sa=0 sb=0 sd=0 mult=1 m=1
XMBP PB PB VDD VDD sky130_fd_pr__pfet_g5v0d10v5 L=4 W=10 nf=1 ad='int((1 + 1)/2) * 10 / 1 * 0.29' as='int((1 + 2)/2) * 10 / 1 * 0.29'
+ pd='2*int((1 + 1)/2) * (10 / 1 + 0.29)' ps='2*int((1 + 2)/2) * (10 / 1 + 0.29)' nrd='0.29 / 10 ' nrs='0.29 / 10 '
+ sa=0 sb=0 sd=0 mult=1 m=1
XMBN2 PCAS NBG VSS VSS sky130_fd_pr__nfet_g5v0d10v5 L=2 W=4 nf=1 ad='int((1 + 1)/2) * 4 / 1 * 0.29' as='int((1 + 2)/2) * 4 / 1 * 0.29'
+ pd='2*int((1 + 1)/2) * (4 / 1 + 0.29)' ps='2*int((1 + 2)/2) * (4 / 1 + 0.29)' nrd='0.29 / 4 ' nrs='0.29 / 4 '
+ sa=0 sb=0 sd=0 mult=1 m=1
XMCB PCAS PCAS VDD VDD sky130_fd_pr__pfet_g5v0d10v5 L=8 W=1 nf=1 ad='int((1 + 1)/2) * 1 / 1 * 0.29' as='int((1 + 2)/2) * 1 / 1 * 0.29'
+ pd='2*int((1 + 1)/2) * (1 / 1 + 0.29)' ps='2*int((1 + 2)/2) * (1 / 1 + 0.29)' nrd='0.29 / 1 ' nrs='0.29 / 1 '
+ sa=0 sb=0 sd=0 mult=1 m=1
XMINVP ENB EN VDD VDD sky130_fd_pr__pfet_g5v0d10v5 L=0.5 W=2 nf=1 ad='int((1 + 1)/2) * 2 / 1 * 0.29'
+ as='int((1 + 2)/2) * 2 / 1 * 0.29' pd='2*int((1 + 1)/2) * (2 / 1 + 0.29)' ps='2*int((1 + 2)/2) * (2 / 1 + 0.29)'
+ nrd='0.29 / 2 ' nrs='0.29 / 2 ' sa=0 sb=0 sd=0 mult=1 m=1
XMINVN ENB EN VSS VSS sky130_fd_pr__nfet_g5v0d10v5 L=0.5 W=1 nf=1 ad='int((1 + 1)/2) * 1 / 1 * 0.29'
+ as='int((1 + 2)/2) * 1 / 1 * 0.29' pd='2*int((1 + 1)/2) * (1 / 1 + 0.29)' ps='2*int((1 + 2)/2) * (1 / 1 + 0.29)'
+ nrd='0.29 / 1 ' nrs='0.29 / 1 ' sa=0 sb=0 sd=0 mult=1 m=1
XMT NT PB VDD VDD sky130_fd_pr__pfet_g5v0d10v5 L=4 W=20 nf=1 ad='int((1 + 1)/2) * 20 / 1 * 0.29' as='int((1 + 2)/2) * 20 / 1 * 0.29'
+ pd='2*int((1 + 1)/2) * (20 / 1 + 0.29)' ps='2*int((1 + 2)/2) * (20 / 1 + 0.29)' nrd='0.29 / 20 ' nrs='0.29 / 20 '
+ sa=0 sb=0 sd=0 mult=1 m=1
XMI1 N1 NA NT NT sky130_fd_pr__pfet_g5v0d10v5 L=4 W=32 nf=1 ad='int((1 + 1)/2) * 32 / 1 * 0.29' as='int((1 + 2)/2) * 32 / 1 * 0.29'
+ pd='2*int((1 + 1)/2) * (32 / 1 + 0.29)' ps='2*int((1 + 2)/2) * (32 / 1 + 0.29)' nrd='0.29 / 32 ' nrs='0.29 / 32 '
+ sa=0 sb=0 sd=0 mult=1 m=1
XMI2 N2 NB NT NT sky130_fd_pr__pfet_g5v0d10v5 L=4 W=32 nf=1 ad='int((1 + 1)/2) * 32 / 1 * 0.29' as='int((1 + 2)/2) * 32 / 1 * 0.29'
+ pd='2*int((1 + 1)/2) * (32 / 1 + 0.29)' ps='2*int((1 + 2)/2) * (32 / 1 + 0.29)' nrd='0.29 / 32 ' nrs='0.29 / 32 '
+ sa=0 sb=0 sd=0 mult=1 m=1
XML1 N1 N1 VSS VSS sky130_fd_pr__nfet_g5v0d10v5 L=8 W=8 nf=1 ad='int((1 + 1)/2) * 8 / 1 * 0.29' as='int((1 + 2)/2) * 8 / 1 * 0.29'
+ pd='2*int((1 + 1)/2) * (8 / 1 + 0.29)' ps='2*int((1 + 2)/2) * (8 / 1 + 0.29)' nrd='0.29 / 8 ' nrs='0.29 / 8 '
+ sa=0 sb=0 sd=0 mult=1 m=1
XML2 N2 N1 VSS VSS sky130_fd_pr__nfet_g5v0d10v5 L=8 W=8 nf=1 ad='int((1 + 1)/2) * 8 / 1 * 0.29' as='int((1 + 2)/2) * 8 / 1 * 0.29'
+ pd='2*int((1 + 1)/2) * (8 / 1 + 0.29)' ps='2*int((1 + 2)/2) * (8 / 1 + 0.29)' nrd='0.29 / 8 ' nrs='0.29 / 8 '
+ sa=0 sb=0 sd=0 mult=1 m=1
XMS2N PG N2 VSS VSS sky130_fd_pr__nfet_g5v0d10v5 L=8 W=8 nf=1 ad='int((1 + 1)/2) * 8 / 1 * 0.29' as='int((1 + 2)/2) * 8 / 1 * 0.29'
+ pd='2*int((1 + 1)/2) * (8 / 1 + 0.29)' ps='2*int((1 + 2)/2) * (8 / 1 + 0.29)' nrd='0.29 / 8 ' nrs='0.29 / 8 '
+ sa=0 sb=0 sd=0 mult=1 m=1
XMS2P PG PB VDD VDD sky130_fd_pr__pfet_g5v0d10v5 L=4 W=10 nf=1 ad='int((1 + 1)/2) * 10 / 1 * 0.29' as='int((1 + 2)/2) * 10 / 1 * 0.29'
+ pd='2*int((1 + 1)/2) * (10 / 1 + 0.29)' ps='2*int((1 + 2)/2) * (10 / 1 + 0.29)' nrd='0.29 / 10 ' nrs='0.29 / 10 '
+ sa=0 sb=0 sd=0 mult=1 m=1
XCC PG NZ sky130_fd_pr__cap_mim_m3_1 W=12 L=12 MF=1 m=1
XRZ NZ N2 VSS sky130_fd_pr__res_xhigh_po W=2 L=1000 mult=1 m=1
XMP1 M1D PG VDD VDD sky130_fd_pr__pfet_g5v0d10v5 L=4 W=8 nf=1 ad='int((1 + 1)/2) * 8 / 1 * 0.29' as='int((1 + 2)/2) * 8 / 1 * 0.29'
+ pd='2*int((1 + 1)/2) * (8 / 1 + 0.29)' ps='2*int((1 + 2)/2) * (8 / 1 + 0.29)' nrd='0.29 / 8 ' nrs='0.29 / 8 '
+ sa=0 sb=0 sd=0 mult=1 m=1
XMPC1 NA PCAS M1D VDD sky130_fd_pr__pfet_g5v0d10v5 L=1 W=8 nf=1 ad='int((1 + 1)/2) * 8 / 1 * 0.29' as='int((1 + 2)/2) * 8 / 1 * 0.29'
+ pd='2*int((1 + 1)/2) * (8 / 1 + 0.29)' ps='2*int((1 + 2)/2) * (8 / 1 + 0.29)' nrd='0.29 / 8 ' nrs='0.29 / 8 '
+ sa=0 sb=0 sd=0 mult=1 m=1
XMP2 M2D PG VDD VDD sky130_fd_pr__pfet_g5v0d10v5 L=4 W=8 nf=1 ad='int((1 + 1)/2) * 8 / 1 * 0.29' as='int((1 + 2)/2) * 8 / 1 * 0.29'
+ pd='2*int((1 + 1)/2) * (8 / 1 + 0.29)' ps='2*int((1 + 2)/2) * (8 / 1 + 0.29)' nrd='0.29 / 8 ' nrs='0.29 / 8 '
+ sa=0 sb=0 sd=0 mult=1 m=1
XMPC2 NB PCAS M2D VDD sky130_fd_pr__pfet_g5v0d10v5 L=1 W=8 nf=1 ad='int((1 + 1)/2) * 8 / 1 * 0.29' as='int((1 + 2)/2) * 8 / 1 * 0.29'
+ pd='2*int((1 + 1)/2) * (8 / 1 + 0.29)' ps='2*int((1 + 2)/2) * (8 / 1 + 0.29)' nrd='0.29 / 8 ' nrs='0.29 / 8 '
+ sa=0 sb=0 sd=0 mult=1 m=1
XMP3 M3D PG VDD VDD sky130_fd_pr__pfet_g5v0d10v5 L=4 W=8 nf=1 ad='int((1 + 1)/2) * 8 / 1 * 0.29' as='int((1 + 2)/2) * 8 / 1 * 0.29'
+ pd='2*int((1 + 1)/2) * (8 / 1 + 0.29)' ps='2*int((1 + 2)/2) * (8 / 1 + 0.29)' nrd='0.29 / 8 ' nrs='0.29 / 8 '
+ sa=0 sb=0 sd=0 mult=1 m=1
XMPC3 PTAT PCAS M3D VDD sky130_fd_pr__pfet_g5v0d10v5 L=1 W=8 nf=1 ad='int((1 + 1)/2) * 8 / 1 * 0.29'
+ as='int((1 + 2)/2) * 8 / 1 * 0.29' pd='2*int((1 + 1)/2) * (8 / 1 + 0.29)' ps='2*int((1 + 2)/2) * (8 / 1 + 0.29)'
+ nrd='0.29 / 8 ' nrs='0.29 / 8 ' sa=0 sb=0 sd=0 mult=1 m=1
XMSU1 ND PB VDD VDD sky130_fd_pr__pfet_g5v0d10v5 L=8 W=1 nf=1 ad='int((1 + 1)/2) * 1 / 1 * 0.29' as='int((1 + 2)/2) * 1 / 1 * 0.29'
+ pd='2*int((1 + 1)/2) * (1 / 1 + 0.29)' ps='2*int((1 + 2)/2) * (1 / 1 + 0.29)' nrd='0.29 / 1 ' nrs='0.29 / 1 '
+ sa=0 sb=0 sd=0 mult=1 m=1
XMSU2 ND NR VSS VSS sky130_fd_pr__nfet_g5v0d10v5 L=2 W=2 nf=1 ad='int((1 + 1)/2) * 2 / 1 * 0.29' as='int((1 + 2)/2) * 2 / 1 * 0.29'
+ pd='2*int((1 + 1)/2) * (2 / 1 + 0.29)' ps='2*int((1 + 2)/2) * (2 / 1 + 0.29)' nrd='0.29 / 2 ' nrs='0.29 / 2 '
+ sa=0 sb=0 sd=0 mult=1 m=1
XMSU3 PG ND VSS VSS sky130_fd_pr__nfet_g5v0d10v5 L=1 W=4 nf=1 ad='int((1 + 1)/2) * 4 / 1 * 0.29' as='int((1 + 2)/2) * 4 / 1 * 0.29'
+ pd='2*int((1 + 1)/2) * (4 / 1 + 0.29)' ps='2*int((1 + 2)/2) * (4 / 1 + 0.29)' nrd='0.29 / 4 ' nrs='0.29 / 4 '
+ sa=0 sb=0 sd=0 mult=1 m=1
XMDND ND ENB VSS VSS sky130_fd_pr__nfet_g5v0d10v5 L=0.5 W=2 nf=1 ad='int((1 + 1)/2) * 2 / 1 * 0.29' as='int((1 + 2)/2) * 2 / 1 * 0.29'
+ pd='2*int((1 + 1)/2) * (2 / 1 + 0.29)' ps='2*int((1 + 2)/2) * (2 / 1 + 0.29)' nrd='0.29 / 2 ' nrs='0.29 / 2 '
+ sa=0 sb=0 sd=0 mult=1 m=1
XMENPG PG EN VDD VDD sky130_fd_pr__pfet_g5v0d10v5 L=0.5 W=4 nf=1 ad='int((1 + 1)/2) * 4 / 1 * 0.29' as='int((1 + 2)/2) * 4 / 1 * 0.29'
+ pd='2*int((1 + 1)/2) * (4 / 1 + 0.29)' ps='2*int((1 + 2)/2) * (4 / 1 + 0.29)' nrd='0.29 / 4 ' nrs='0.29 / 4 '
+ sa=0 sb=0 sd=0 mult=1 m=1
XMENPT PTAT ENB VSS VSS sky130_fd_pr__nfet_g5v0d10v5 L=1 W=1 nf=1 ad='int((1 + 1)/2) * 1 / 1 * 0.29'
+ as='int((1 + 2)/2) * 1 / 1 * 0.29' pd='2*int((1 + 1)/2) * (1 / 1 + 0.29)' ps='2*int((1 + 2)/2) * (1 / 1 + 0.29)'
+ nrd='0.29 / 1 ' nrs='0.29 / 1 ' sa=0 sb=0 sd=0 mult=1 m=1
XMENCT CTAT ENB VSS VSS sky130_fd_pr__nfet_g5v0d10v5 L=1 W=1 nf=1 ad='int((1 + 1)/2) * 1 / 1 * 0.29'
+ as='int((1 + 2)/2) * 1 / 1 * 0.29' pd='2*int((1 + 1)/2) * (1 / 1 + 0.29)' ps='2*int((1 + 2)/2) * (1 / 1 + 0.29)'
+ nrd='0.29 / 1 ' nrs='0.29 / 1 ' sa=0 sb=0 sd=0 mult=1 m=1
XMSU4 NR PG VDD VDD sky130_fd_pr__pfet_g5v0d10v5 L=4 W=1 nf=1 ad='int((1 + 1)/2) * 1 / 1 * 0.29' as='int((1 + 2)/2) * 1 / 1 * 0.29'
+ pd='2*int((1 + 1)/2) * (1 / 1 + 0.29)' ps='2*int((1 + 2)/2) * (1 / 1 + 0.29)' nrd='0.29 / 1 ' nrs='0.29 / 1 '
+ sa=0 sb=0 sd=0 mult=1 m=1
XMSU5 NR NR VSS VSS sky130_fd_pr__nfet_g5v0d10v5 L=2 W=2 nf=1 ad='int((1 + 1)/2) * 2 / 1 * 0.29' as='int((1 + 2)/2) * 2 / 1 * 0.29'
+ pd='2*int((1 + 1)/2) * (2 / 1 + 0.29)' ps='2*int((1 + 2)/2) * (2 / 1 + 0.29)' nrd='0.29 / 2 ' nrs='0.29 / 2 '
+ sa=0 sb=0 sd=0 mult=1 m=1
XMDN2 N2 ENB VSS VSS sky130_fd_pr__nfet_g5v0d10v5 L=1 W=2 nf=1 ad='int((1 + 1)/2) * 2 / 1 * 0.29' as='int((1 + 2)/2) * 2 / 1 * 0.29'
+ pd='2*int((1 + 1)/2) * (2 / 1 + 0.29)' ps='2*int((1 + 2)/2) * (2 / 1 + 0.29)' nrd='0.29 / 2 ' nrs='0.29 / 2 '
+ sa=0 sb=0 sd=0 mult=1 m=1
XMDNT NT ENB VSS VSS sky130_fd_pr__nfet_g5v0d10v5 L=1 W=2 nf=1 ad='int((1 + 1)/2) * 2 / 1 * 0.29' as='int((1 + 2)/2) * 2 / 1 * 0.29'
+ pd='2*int((1 + 1)/2) * (2 / 1 + 0.29)' ps='2*int((1 + 2)/2) * (2 / 1 + 0.29)' nrd='0.29 / 2 ' nrs='0.29 / 2 '
+ sa=0 sb=0 sd=0 mult=1 m=1
XQ1 VSS VSS NA sky130_fd_pr__pnp_05v5_W3p40L3p40 m=1
XQ8A VSS VSS NC sky130_fd_pr__pnp_05v5_W3p40L3p40 m=1
XQ8B VSS VSS NC sky130_fd_pr__pnp_05v5_W3p40L3p40 m=1
XQ8C VSS VSS NC sky130_fd_pr__pnp_05v5_W3p40L3p40 m=1
XQ8D VSS VSS NC sky130_fd_pr__pnp_05v5_W3p40L3p40 m=1
XQ8E VSS VSS NC sky130_fd_pr__pnp_05v5_W3p40L3p40 m=1
XQ8F VSS VSS NC sky130_fd_pr__pnp_05v5_W3p40L3p40 m=1
XQ8G VSS VSS NC sky130_fd_pr__pnp_05v5_W3p40L3p40 m=1
XQ8H VSS VSS NC sky130_fd_pr__pnp_05v5_W3p40L3p40 m=1
XR1 NB NC VSS sky130_fd_pr__res_xhigh_po W=2 L=119.47 mult=1 m=1
XR2 PTAT PTAT_TRIM VSS sky130_fd_pr__res_xhigh_po W=2 L=2652.6 mult=1 m=1
XR2TRIM PTAT_TRIM VSS VSS sky130_fd_pr__res_xhigh_po W=2 L=450.88 mult=1 m=1
XRISO NA CTAT VSS sky130_fd_pr__res_xhigh_po W=2 L=111.05 mult=1 m=1
.ends

.end
